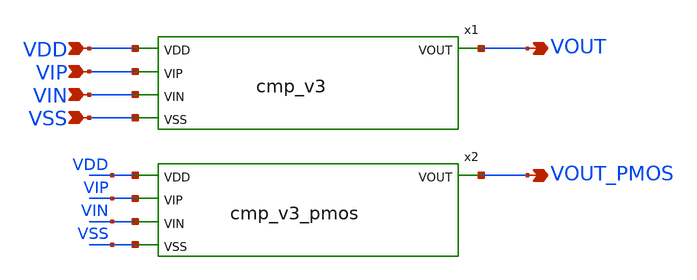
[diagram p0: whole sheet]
** sch_path: design/LELO_TORD_SKY130A/TB_cmp_gain.sch
**.subckt TB_cmp_gain VOUT VDD VIP VIN VSS VOUT_PMOS
*.opin VOUT
*.ipin VDD
*.ipin VIP
*.ipin VIN
*.ipin VSS
*.opin VOUT_PMOS
x1 VDD VIP VIN VOUT VSS cmp_v3
x2 VDD VIP VIN VOUT_PMOS VSS cmp_v3_pmos
**.ends
.end
